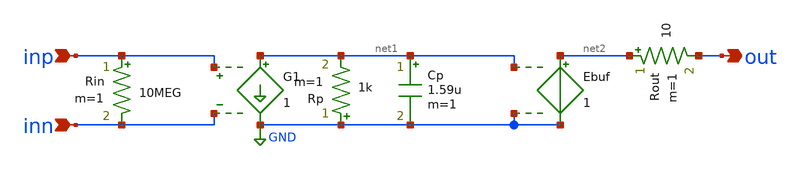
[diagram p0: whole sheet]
** sch_path: prj/template/2_Idealized_circuits/opamp1.sch
**.subckt opamp1 inp inn out
*.ipin inp
*.ipin inn
*.opin out
Rin inp inn 10MEG m=1
Rout net2 out 10 m=1
Cp net1 GND 1.59u m=1
Rp GND net1 1k m=1
Ebuf net2 GND net1 GND 1
G1 net1 GND inp inn 1
**.ends
.GLOBAL GND
.end
